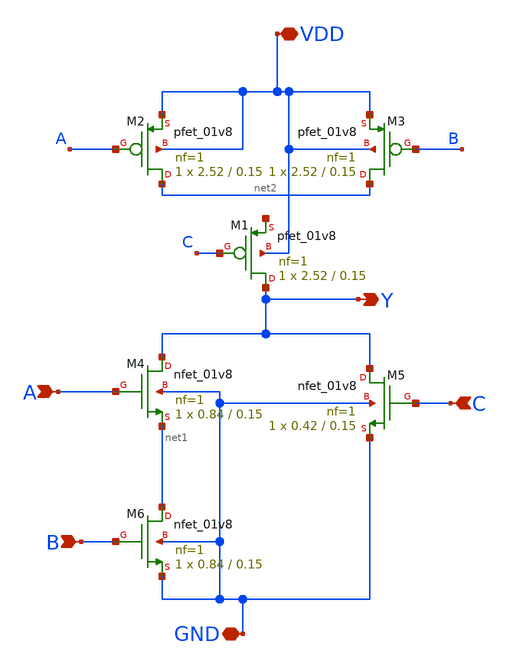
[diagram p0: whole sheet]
** sch_path: cells/AOI3X1/schematic/aoi3x1.sch
**.subckt aoi3x1 VDD GND A B C Y
*.iopin VDD
*.iopin GND
*.ipin A
*.ipin B
*.ipin C
*.opin Y
XM1 Y C net3 VDD sky130_fd_pr__pfet_01v8 L=0.15 W=2.52 nf=1 ad='int((1 + 1)/2) * 2.52 / 1 * 0.29' as='int((1 + 2)/2) * 2.52 / 1 * 0.29'
+ pd='2*int((1 + 1)/2) * (2.52 / 1 + 0.29)' ps='2*int((1 + 2)/2) * (2.52 / 1 + 0.29)' nrd='0.29 / 2.52 '
+ nrs='0.29 / 2.52 ' sa=0 sb=0 sd=0 mult=1 m=1
XM2 net2 A VDD VDD sky130_fd_pr__pfet_01v8 L=0.15 W=2.52 nf=1 ad='int((1 + 1)/2) * 2.52 / 1 * 0.29' as='int((1 + 2)/2) * 2.52 / 1 * 0.29'
+ pd='2*int((1 + 1)/2) * (2.52 / 1 + 0.29)' ps='2*int((1 + 2)/2) * (2.52 / 1 + 0.29)' nrd='0.29 / 2.52 '
+ nrs='0.29 / 2.52 ' sa=0 sb=0 sd=0 mult=1 m=1
XM3 net2 B VDD VDD sky130_fd_pr__pfet_01v8 L=0.15 W=2.52 nf=1 ad='int((1 + 1)/2) * 2.52 / 1 * 0.29' as='int((1 + 2)/2) * 2.52 / 1 * 0.29'
+ pd='2*int((1 + 1)/2) * (2.52 / 1 + 0.29)' ps='2*int((1 + 2)/2) * (2.52 / 1 + 0.29)' nrd='0.29 / 2.52 '
+ nrs='0.29 / 2.52 ' sa=0 sb=0 sd=0 mult=1 m=1
XM4 Y A net1 GND sky130_fd_pr__nfet_01v8 L=0.15 W=0.84 nf=1 ad='int((1 + 1)/2) * 0.84 / 1 * 0.29' as='int((1 + 2)/2) * 0.84 / 1 * 0.29'
+ pd='2*int((1 + 1)/2) * (0.84 / 1 + 0.29)' ps='2*int((1 + 2)/2) * (0.84 / 1 + 0.29)' nrd='0.29 / 0.84 '
+ nrs='0.29 / 0.84 ' sa=0 sb=0 sd=0 mult=1 m=1
XM5 Y C GND GND sky130_fd_pr__nfet_01v8 L=0.15 W=0.42 nf=1 ad='int((1 + 1)/2) * 0.42 / 1 * 0.29' as='int((1 + 2)/2) * 0.42 / 1 * 0.29'
+ pd='2*int((1 + 1)/2) * (0.42 / 1 + 0.29)' ps='2*int((1 + 2)/2) * (0.42 / 1 + 0.29)' nrd='0.29 / 0.42 '
+ nrs='0.29 / 0.42 ' sa=0 sb=0 sd=0 mult=1 m=1
XM6 net1 B GND GND sky130_fd_pr__nfet_01v8 L=0.15 W=0.84 nf=1 ad='int((1 + 1)/2) * 0.84 / 1 * 0.29' as='int((1 + 2)/2) * 0.84 / 1 * 0.29'
+ pd='2*int((1 + 1)/2) * (0.84 / 1 + 0.29)' ps='2*int((1 + 2)/2) * (0.84 / 1 + 0.29)' nrd='0.29 / 0.84 '
+ nrs='0.29 / 0.84 ' sa=0 sb=0 sd=0 mult=1 m=1
**.ends
.end
